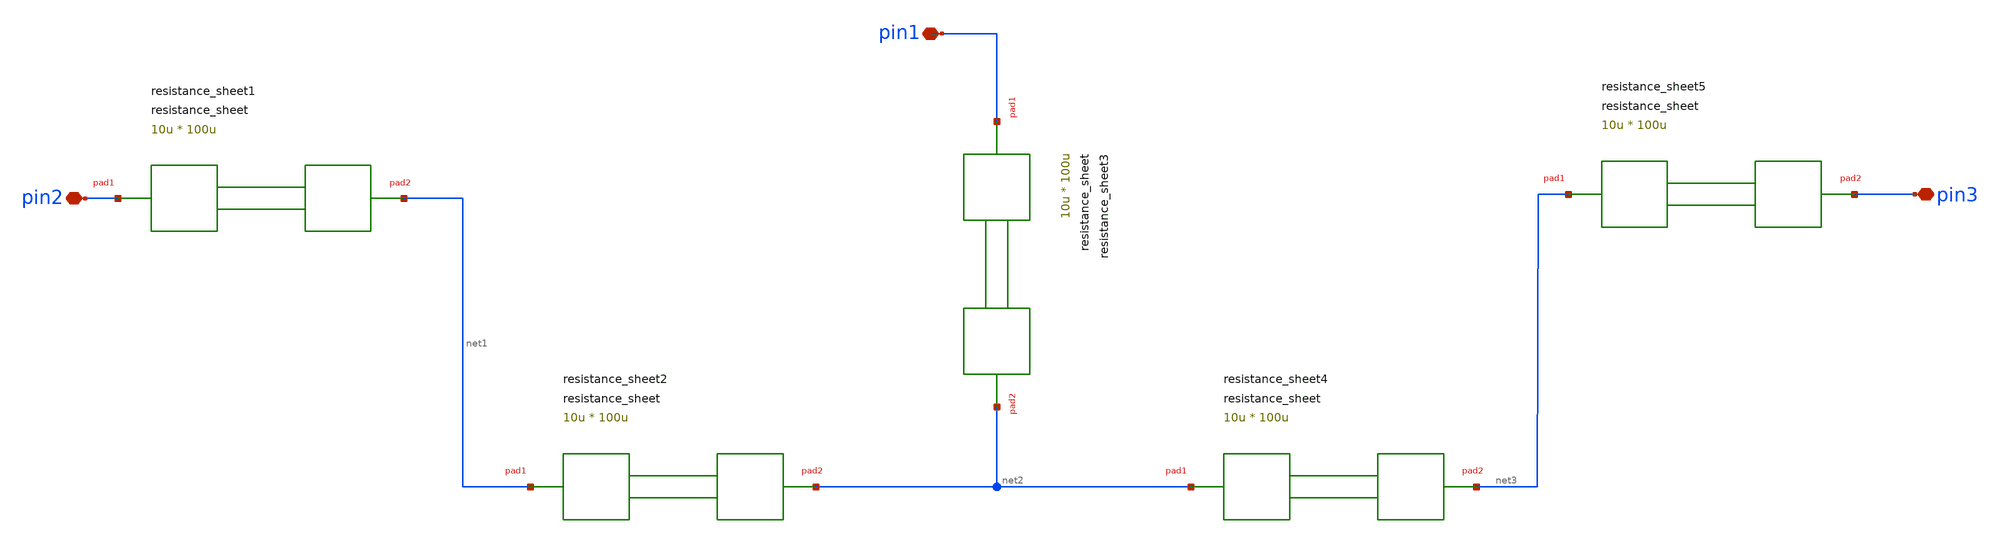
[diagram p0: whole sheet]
** sch_path: xschem/tests/test_sch/test_resistance_sheet.sch
* Copyright (c) 2024, Mabrains LLC
* Licensed under the GNU Lesser General Public License, Version 3.0 (the "License");
* you may not use this file except in compliance with the License.
* GNU Lesser General Public License
* Version 3, 29 June 2007
* This program is free software: you can redistribute it and/or modify
* it under the terms of the GNU Lesser General Public License as published
* by the Free Software Foundation, either version 3 of the License, or
* (at your option) any later version.
* This program is distributed in the hope that it will be useful,
* but WITHOUT ANY WARRANTY; without even the implied warranty of
* MERCHANTABILITY or FITNESS FOR A PARTICULAR PURPOSE.  See the
* GNU Lesser General Public License for more details.
* You should have received a copy of the GNU Lesser General Public License
* along with this program.  If not, see <https://www.gnu.org/licenses/>.
* SPDX-License-Identifier: LGPL-3.0
**.subckt test_resistance_sheet pin2 pin1 pin3
*.iopin pin2
*.iopin pin1
*.iopin pin3
Presistance_sheet1 pin2 net1 resistance_sheet width=10u pad_pitch=100u
Presistance_sheet2 net1 net2 resistance_sheet width=10u pad_pitch=100u
Presistance_sheet3 pin1 net2 resistance_sheet width=10u pad_pitch=100u
Presistance_sheet4 net2 net3 resistance_sheet width=10u pad_pitch=100u
Presistance_sheet5 net3 pin3 resistance_sheet width=10u pad_pitch=100u
**.ends
.end
